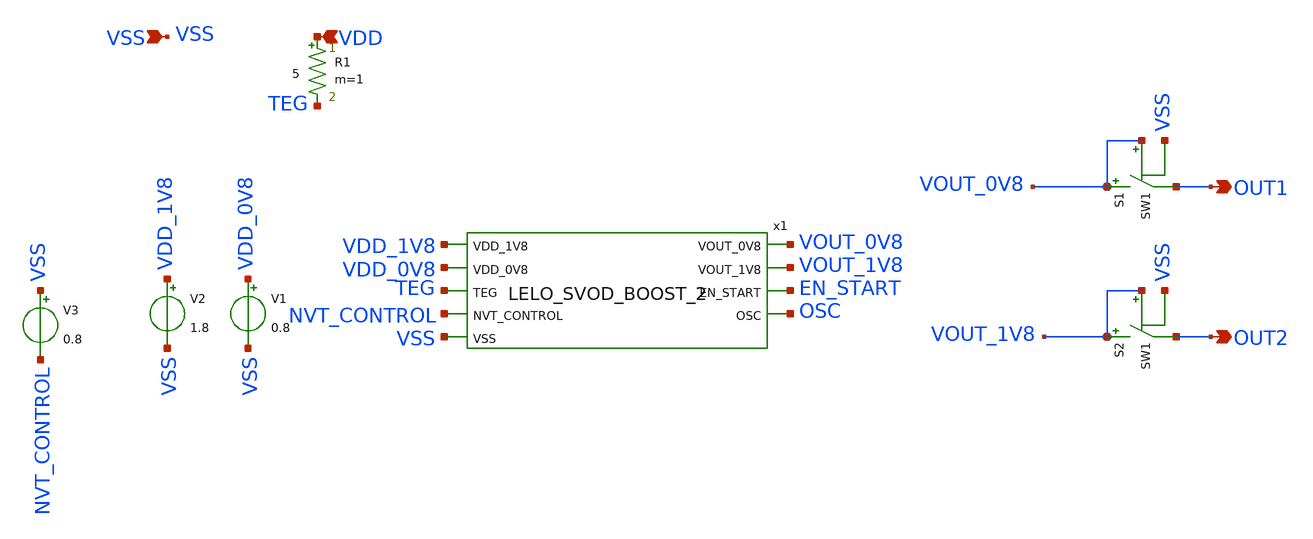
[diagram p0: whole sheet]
** sch_path: design/LELO_SVOD_SKY130A/LELO_SVOD_0V8_BOOST.sch
**.subckt LELO_SVOD_0V8_BOOST VDD VSS OUT2 OUT1
*.ipin VDD
*.ipin VSS
*.opin OUT2
*.opin OUT1
R1 VDD TEG 5 m=1
V1 VDD_0V8 VSS 0.8
V2 VDD_1V8 VSS 1.8
S1 VOUT_0V8 OUT1 VOUT_0V8 VSS SW1
S2 VOUT_1V8 OUT2 VOUT_1V8 VSS SW1
x1 VOUT_0V8 VDD_1V8 VDD_0V8 TEG NVT_CONTROL VSS VOUT_1V8 EN_START OSC LELO_SVOD_BOOST_2
V3 VSS NVT_CONTROL 0.8
**.ends
**** begin user architecture code
.MODEL SW1 SW   VT=0.7 VH=0.001  RON=0.001 ROFF=10G
**** end user architecture code
.end
